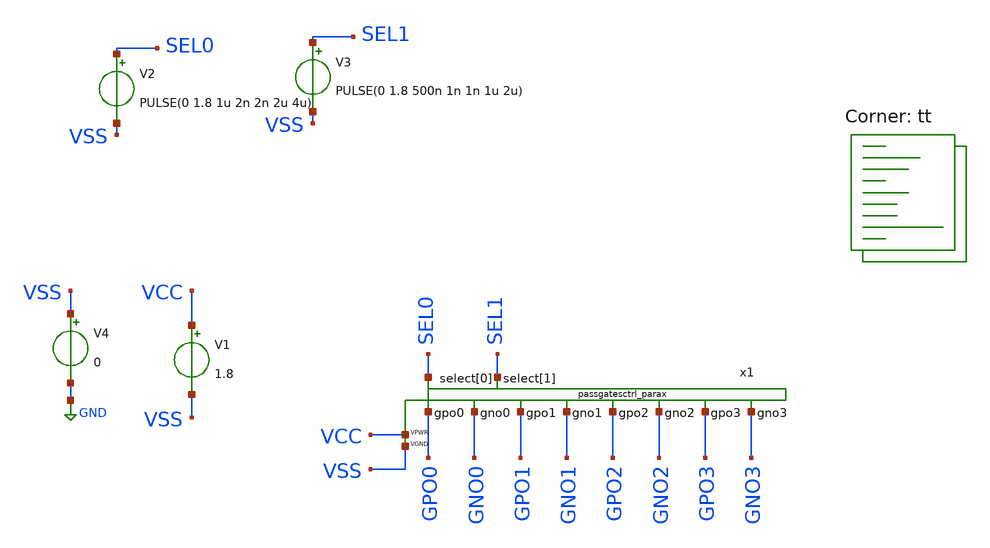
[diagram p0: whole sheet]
** sch_path: xschem/tb_passgatectrl.sch
**.subckt tb_passgatectrl
x1 VSS VCC GNO0 GNO1 GNO2 GNO3 GPO0 GPO1 GPO2 GPO3 SEL0 SEL1 passgatesctrl_parax
V1 VCC VSS 1.8
V2 SEL0 VSS PULSE(0 1.8 1u 2n 2n 2u 4u)
V4 VSS GND 0
V3 SEL1 VSS PULSE(0 1.8 500n 1n 1n 1u 2u)
**** begin user architecture code
.lib $::SKYWATER_MODELS/sky130.lib.spice tt
**** end user architecture code
**.ends
.GLOBAL GND
**** begin user architecture code


* ngspice commands
* .options savecurrents

.control
save all
op
write tb_passgatesctrl.raw
set appendwrite
tran 10n 10u
write tb_passgatesctrl.raw
quit 0
.endc



**** end user architecture code
.end
